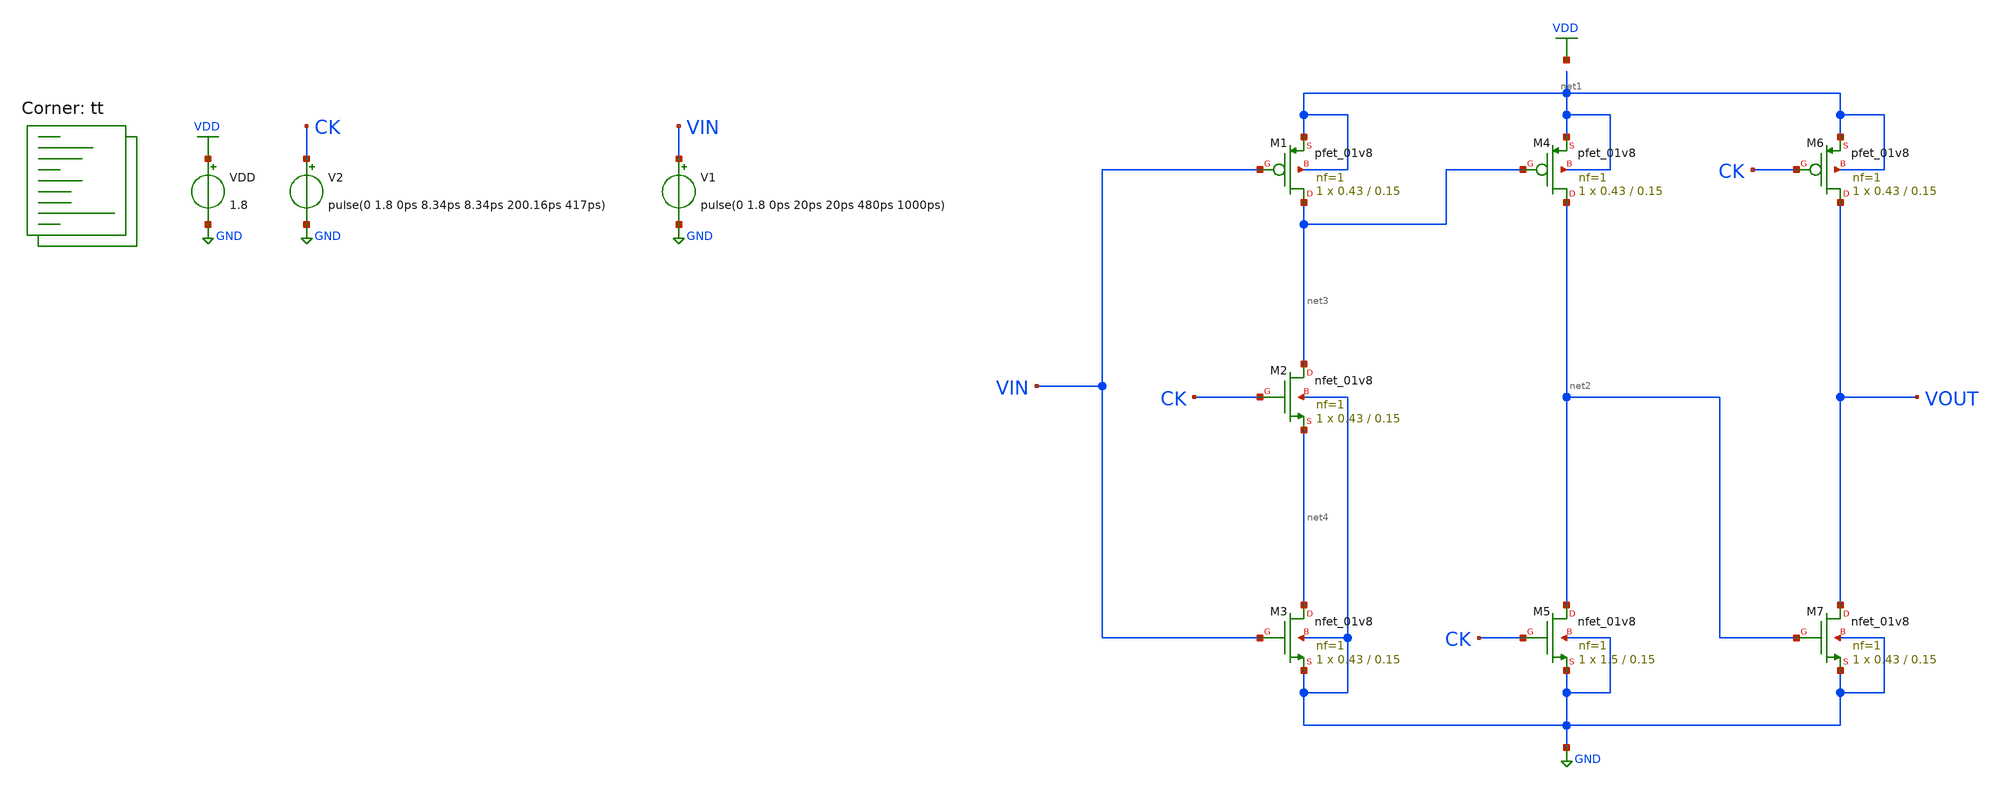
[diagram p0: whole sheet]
** sch_path: projects/pll/divider/xschem_ngspice/tb_TSPC_FF_ratioed.sch
**.subckt tb_TSPC_FF_ratioed
VDD VDD GND 1.8
XM6 VOUT CK net1 net1 sky130_fd_pr__pfet_01v8 L=0.15 W=0.43 nf=1 ad='int((nf+1)/2) * W/nf * 0.29' as='int((nf+2)/2) * W/nf * 0.29'
+ pd='2*int((nf+1)/2) * (W/nf + 0.29)' ps='2*int((nf+2)/2) * (W/nf + 0.29)' nrd='0.29 / W' nrs='0.29 / W'
+ sa=0 sb=0 sd=0 mult=1 m=1
XM7 VOUT net2 GND GND sky130_fd_pr__nfet_01v8 L=0.15 W=0.43 nf=1 ad='int((nf+1)/2) * W/nf * 0.29' as='int((nf+2)/2) * W/nf * 0.29'
+ pd='2*int((nf+1)/2) * (W/nf + 0.29)' ps='2*int((nf+2)/2) * (W/nf + 0.29)' nrd='0.29 / W' nrs='0.29 / W'
+ sa=0 sb=0 sd=0 mult=1 m=1
XM4 net2 net3 net1 net1 sky130_fd_pr__pfet_01v8 L=0.15 W=0.43 nf=1 ad='int((nf+1)/2) * W/nf * 0.29' as='int((nf+2)/2) * W/nf * 0.29'
+ pd='2*int((nf+1)/2) * (W/nf + 0.29)' ps='2*int((nf+2)/2) * (W/nf + 0.29)' nrd='0.29 / W' nrs='0.29 / W'
+ sa=0 sb=0 sd=0 mult=1 m=1
XM5 net2 CK GND GND sky130_fd_pr__nfet_01v8 L=0.15 W=1.5 nf=1 ad='int((nf+1)/2) * W/nf * 0.29' as='int((nf+2)/2) * W/nf * 0.29'
+ pd='2*int((nf+1)/2) * (W/nf + 0.29)' ps='2*int((nf+2)/2) * (W/nf + 0.29)' nrd='0.29 / W' nrs='0.29 / W'
+ sa=0 sb=0 sd=0 mult=1 m=1
XM1 net3 VIN net1 net1 sky130_fd_pr__pfet_01v8 L=0.15 W=0.43 nf=1 ad='int((nf+1)/2) * W/nf * 0.29' as='int((nf+2)/2) * W/nf * 0.29'
+ pd='2*int((nf+1)/2) * (W/nf + 0.29)' ps='2*int((nf+2)/2) * (W/nf + 0.29)' nrd='0.29 / W' nrs='0.29 / W'
+ sa=0 sb=0 sd=0 mult=1 m=1
XM3 net4 VIN GND GND sky130_fd_pr__nfet_01v8 L=0.15 W=0.43 nf=1 ad='int((nf+1)/2) * W/nf * 0.29' as='int((nf+2)/2) * W/nf * 0.29'
+ pd='2*int((nf+1)/2) * (W/nf + 0.29)' ps='2*int((nf+2)/2) * (W/nf + 0.29)' nrd='0.29 / W' nrs='0.29 / W'
+ sa=0 sb=0 sd=0 mult=1 m=1
XM2 net3 CK net4 GND sky130_fd_pr__nfet_01v8 L=0.15 W=0.43 nf=1 ad='int((nf+1)/2) * W/nf * 0.29' as='int((nf+2)/2) * W/nf * 0.29'
+ pd='2*int((nf+1)/2) * (W/nf + 0.29)' ps='2*int((nf+2)/2) * (W/nf + 0.29)' nrd='0.29 / W' nrs='0.29 / W'
+ sa=0 sb=0 sd=0 mult=1 m=1
V2 CK GND pulse(0 1.8 0ps 8.34ps 8.34ps 200.16ps 417ps)
V1 VIN GND pulse(0 1.8 0ps 20ps 20ps 480ps 1000ps)
**** begin user architecture code



.option method=gear
.option wnflag=1

.control

  save all
  tran 5p 20n
  remzerovec
  write tb_TSPC_FF_ratioed.raw
  set appendwrite

.endc



.lib $::SKYWATER_MODELS/sky130.lib.spice tt
**** end user architecture code
**.ends
.GLOBAL GND
.GLOBAL VDD
.end
